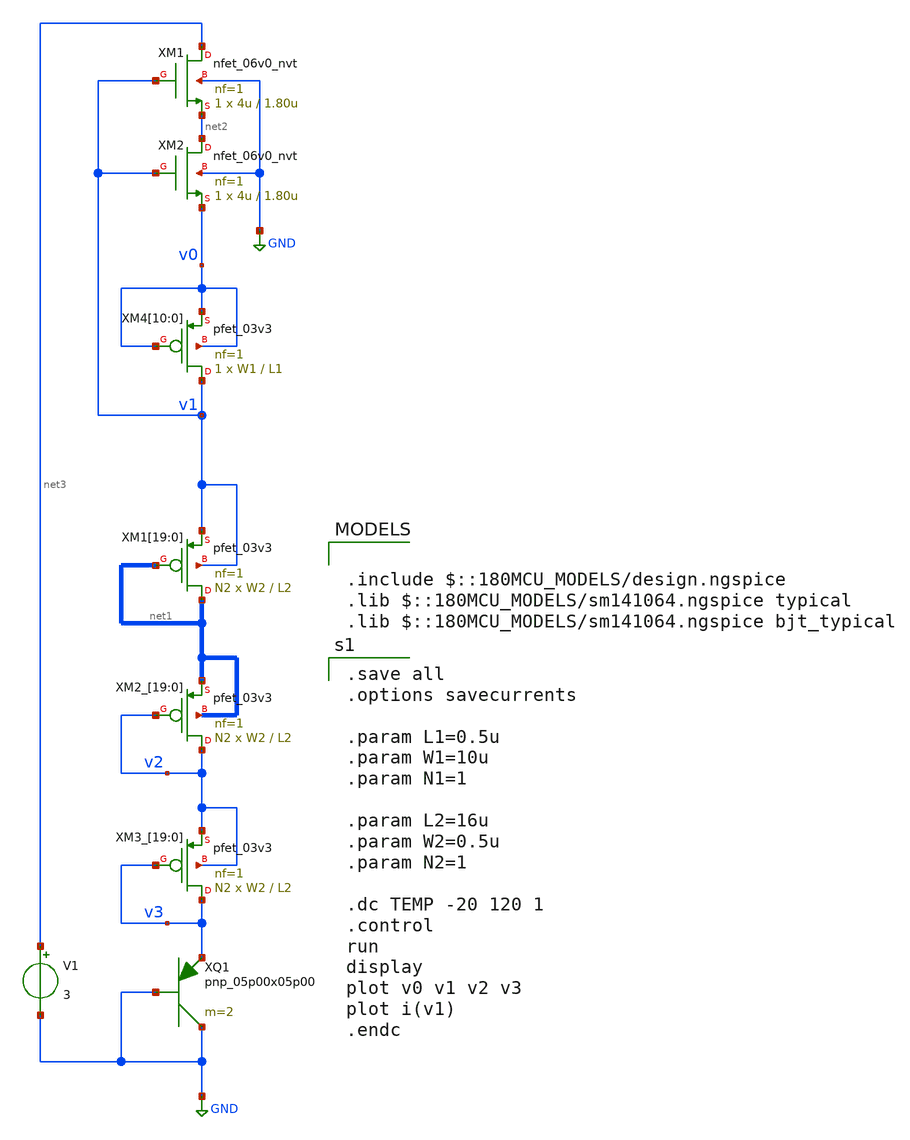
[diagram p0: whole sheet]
** sch_path: GF180/xschem/cmos_vref/Y.Ji_JSSC2019/s2_ztat1.sch
**.subckt s2_ztat1
XQ1 GND GND v3 pnp_05p00x05p00 m=2
V1 net3 GND 3
XM4[10] v1 v0 v0 v0 pfet_03v3 L=L1 W=W1 nf=1 ad='int((nf+1)/2) * W/nf * 0.18u' as='int((nf+2)/2) * W/nf * 0.18u'
+ pd='2*int((nf+1)/2) * (W/nf + 0.18u)' ps='2*int((nf+2)/2) * (W/nf + 0.18u)' nrd='0.18u / W' nrs='0.18u / W'
+ sa=0 sb=0 sd=0 m=1
XM4[9] v1 v0 v0 v0 pfet_03v3 L=L1 W=W1 nf=1 ad='int((nf+1)/2) * W/nf * 0.18u' as='int((nf+2)/2) * W/nf * 0.18u'
+ pd='2*int((nf+1)/2) * (W/nf + 0.18u)' ps='2*int((nf+2)/2) * (W/nf + 0.18u)' nrd='0.18u / W' nrs='0.18u / W'
+ sa=0 sb=0 sd=0 m=1
XM4[8] v1 v0 v0 v0 pfet_03v3 L=L1 W=W1 nf=1 ad='int((nf+1)/2) * W/nf * 0.18u' as='int((nf+2)/2) * W/nf * 0.18u'
+ pd='2*int((nf+1)/2) * (W/nf + 0.18u)' ps='2*int((nf+2)/2) * (W/nf + 0.18u)' nrd='0.18u / W' nrs='0.18u / W'
+ sa=0 sb=0 sd=0 m=1
XM4[7] v1 v0 v0 v0 pfet_03v3 L=L1 W=W1 nf=1 ad='int((nf+1)/2) * W/nf * 0.18u' as='int((nf+2)/2) * W/nf * 0.18u'
+ pd='2*int((nf+1)/2) * (W/nf + 0.18u)' ps='2*int((nf+2)/2) * (W/nf + 0.18u)' nrd='0.18u / W' nrs='0.18u / W'
+ sa=0 sb=0 sd=0 m=1
XM4[6] v1 v0 v0 v0 pfet_03v3 L=L1 W=W1 nf=1 ad='int((nf+1)/2) * W/nf * 0.18u' as='int((nf+2)/2) * W/nf * 0.18u'
+ pd='2*int((nf+1)/2) * (W/nf + 0.18u)' ps='2*int((nf+2)/2) * (W/nf + 0.18u)' nrd='0.18u / W' nrs='0.18u / W'
+ sa=0 sb=0 sd=0 m=1
XM4[5] v1 v0 v0 v0 pfet_03v3 L=L1 W=W1 nf=1 ad='int((nf+1)/2) * W/nf * 0.18u' as='int((nf+2)/2) * W/nf * 0.18u'
+ pd='2*int((nf+1)/2) * (W/nf + 0.18u)' ps='2*int((nf+2)/2) * (W/nf + 0.18u)' nrd='0.18u / W' nrs='0.18u / W'
+ sa=0 sb=0 sd=0 m=1
XM4[4] v1 v0 v0 v0 pfet_03v3 L=L1 W=W1 nf=1 ad='int((nf+1)/2) * W/nf * 0.18u' as='int((nf+2)/2) * W/nf * 0.18u'
+ pd='2*int((nf+1)/2) * (W/nf + 0.18u)' ps='2*int((nf+2)/2) * (W/nf + 0.18u)' nrd='0.18u / W' nrs='0.18u / W'
+ sa=0 sb=0 sd=0 m=1
XM4[3] v1 v0 v0 v0 pfet_03v3 L=L1 W=W1 nf=1 ad='int((nf+1)/2) * W/nf * 0.18u' as='int((nf+2)/2) * W/nf * 0.18u'
+ pd='2*int((nf+1)/2) * (W/nf + 0.18u)' ps='2*int((nf+2)/2) * (W/nf + 0.18u)' nrd='0.18u / W' nrs='0.18u / W'
+ sa=0 sb=0 sd=0 m=1
XM4[2] v1 v0 v0 v0 pfet_03v3 L=L1 W=W1 nf=1 ad='int((nf+1)/2) * W/nf * 0.18u' as='int((nf+2)/2) * W/nf * 0.18u'
+ pd='2*int((nf+1)/2) * (W/nf + 0.18u)' ps='2*int((nf+2)/2) * (W/nf + 0.18u)' nrd='0.18u / W' nrs='0.18u / W'
+ sa=0 sb=0 sd=0 m=1
XM4[1] v1 v0 v0 v0 pfet_03v3 L=L1 W=W1 nf=1 ad='int((nf+1)/2) * W/nf * 0.18u' as='int((nf+2)/2) * W/nf * 0.18u'
+ pd='2*int((nf+1)/2) * (W/nf + 0.18u)' ps='2*int((nf+2)/2) * (W/nf + 0.18u)' nrd='0.18u / W' nrs='0.18u / W'
+ sa=0 sb=0 sd=0 m=1
XM4[0] v1 v0 v0 v0 pfet_03v3 L=L1 W=W1 nf=1 ad='int((nf+1)/2) * W/nf * 0.18u' as='int((nf+2)/2) * W/nf * 0.18u'
+ pd='2*int((nf+1)/2) * (W/nf + 0.18u)' ps='2*int((nf+2)/2) * (W/nf + 0.18u)' nrd='0.18u / W' nrs='0.18u / W'
+ sa=0 sb=0 sd=0 m=1
XM2_[19] v2 v2 net1[19] net1[19] pfet_03v3 L=L2 W=W2 nf=1 ad='int((nf+1)/2) * W/nf * 0.18u' as='int((nf+2)/2) * W/nf * 0.18u'
+ pd='2*int((nf+1)/2) * (W/nf + 0.18u)' ps='2*int((nf+2)/2) * (W/nf + 0.18u)' nrd='0.18u / W' nrs='0.18u / W'
+ sa=0 sb=0 sd=0 m=N2
XM2_[18] v2 v2 net1[18] net1[18] pfet_03v3 L=L2 W=W2 nf=1 ad='int((nf+1)/2) * W/nf * 0.18u' as='int((nf+2)/2) * W/nf * 0.18u'
+ pd='2*int((nf+1)/2) * (W/nf + 0.18u)' ps='2*int((nf+2)/2) * (W/nf + 0.18u)' nrd='0.18u / W' nrs='0.18u / W'
+ sa=0 sb=0 sd=0 m=N2
XM2_[17] v2 v2 net1[17] net1[17] pfet_03v3 L=L2 W=W2 nf=1 ad='int((nf+1)/2) * W/nf * 0.18u' as='int((nf+2)/2) * W/nf * 0.18u'
+ pd='2*int((nf+1)/2) * (W/nf + 0.18u)' ps='2*int((nf+2)/2) * (W/nf + 0.18u)' nrd='0.18u / W' nrs='0.18u / W'
+ sa=0 sb=0 sd=0 m=N2
XM2_[16] v2 v2 net1[16] net1[16] pfet_03v3 L=L2 W=W2 nf=1 ad='int((nf+1)/2) * W/nf * 0.18u' as='int((nf+2)/2) * W/nf * 0.18u'
+ pd='2*int((nf+1)/2) * (W/nf + 0.18u)' ps='2*int((nf+2)/2) * (W/nf + 0.18u)' nrd='0.18u / W' nrs='0.18u / W'
+ sa=0 sb=0 sd=0 m=N2
XM2_[15] v2 v2 net1[15] net1[15] pfet_03v3 L=L2 W=W2 nf=1 ad='int((nf+1)/2) * W/nf * 0.18u' as='int((nf+2)/2) * W/nf * 0.18u'
+ pd='2*int((nf+1)/2) * (W/nf + 0.18u)' ps='2*int((nf+2)/2) * (W/nf + 0.18u)' nrd='0.18u / W' nrs='0.18u / W'
+ sa=0 sb=0 sd=0 m=N2
XM2_[14] v2 v2 net1[14] net1[14] pfet_03v3 L=L2 W=W2 nf=1 ad='int((nf+1)/2) * W/nf * 0.18u' as='int((nf+2)/2) * W/nf * 0.18u'
+ pd='2*int((nf+1)/2) * (W/nf + 0.18u)' ps='2*int((nf+2)/2) * (W/nf + 0.18u)' nrd='0.18u / W' nrs='0.18u / W'
+ sa=0 sb=0 sd=0 m=N2
XM2_[13] v2 v2 net1[13] net1[13] pfet_03v3 L=L2 W=W2 nf=1 ad='int((nf+1)/2) * W/nf * 0.18u' as='int((nf+2)/2) * W/nf * 0.18u'
+ pd='2*int((nf+1)/2) * (W/nf + 0.18u)' ps='2*int((nf+2)/2) * (W/nf + 0.18u)' nrd='0.18u / W' nrs='0.18u / W'
+ sa=0 sb=0 sd=0 m=N2
XM2_[12] v2 v2 net1[12] net1[12] pfet_03v3 L=L2 W=W2 nf=1 ad='int((nf+1)/2) * W/nf * 0.18u' as='int((nf+2)/2) * W/nf * 0.18u'
+ pd='2*int((nf+1)/2) * (W/nf + 0.18u)' ps='2*int((nf+2)/2) * (W/nf + 0.18u)' nrd='0.18u / W' nrs='0.18u / W'
+ sa=0 sb=0 sd=0 m=N2
XM2_[11] v2 v2 net1[11] net1[11] pfet_03v3 L=L2 W=W2 nf=1 ad='int((nf+1)/2) * W/nf * 0.18u' as='int((nf+2)/2) * W/nf * 0.18u'
+ pd='2*int((nf+1)/2) * (W/nf + 0.18u)' ps='2*int((nf+2)/2) * (W/nf + 0.18u)' nrd='0.18u / W' nrs='0.18u / W'
+ sa=0 sb=0 sd=0 m=N2
XM2_[10] v2 v2 net1[10] net1[10] pfet_03v3 L=L2 W=W2 nf=1 ad='int((nf+1)/2) * W/nf * 0.18u' as='int((nf+2)/2) * W/nf * 0.18u'
+ pd='2*int((nf+1)/2) * (W/nf + 0.18u)' ps='2*int((nf+2)/2) * (W/nf + 0.18u)' nrd='0.18u / W' nrs='0.18u / W'
+ sa=0 sb=0 sd=0 m=N2
XM2_[9] v2 v2 net1[9] net1[9] pfet_03v3 L=L2 W=W2 nf=1 ad='int((nf+1)/2) * W/nf * 0.18u' as='int((nf+2)/2) * W/nf * 0.18u'
+ pd='2*int((nf+1)/2) * (W/nf + 0.18u)' ps='2*int((nf+2)/2) * (W/nf + 0.18u)' nrd='0.18u / W' nrs='0.18u / W'
+ sa=0 sb=0 sd=0 m=N2
XM2_[8] v2 v2 net1[8] net1[8] pfet_03v3 L=L2 W=W2 nf=1 ad='int((nf+1)/2) * W/nf * 0.18u' as='int((nf+2)/2) * W/nf * 0.18u'
+ pd='2*int((nf+1)/2) * (W/nf + 0.18u)' ps='2*int((nf+2)/2) * (W/nf + 0.18u)' nrd='0.18u / W' nrs='0.18u / W'
+ sa=0 sb=0 sd=0 m=N2
XM2_[7] v2 v2 net1[7] net1[7] pfet_03v3 L=L2 W=W2 nf=1 ad='int((nf+1)/2) * W/nf * 0.18u' as='int((nf+2)/2) * W/nf * 0.18u'
+ pd='2*int((nf+1)/2) * (W/nf + 0.18u)' ps='2*int((nf+2)/2) * (W/nf + 0.18u)' nrd='0.18u / W' nrs='0.18u / W'
+ sa=0 sb=0 sd=0 m=N2
XM2_[6] v2 v2 net1[6] net1[6] pfet_03v3 L=L2 W=W2 nf=1 ad='int((nf+1)/2) * W/nf * 0.18u' as='int((nf+2)/2) * W/nf * 0.18u'
+ pd='2*int((nf+1)/2) * (W/nf + 0.18u)' ps='2*int((nf+2)/2) * (W/nf + 0.18u)' nrd='0.18u / W' nrs='0.18u / W'
+ sa=0 sb=0 sd=0 m=N2
XM2_[5] v2 v2 net1[5] net1[5] pfet_03v3 L=L2 W=W2 nf=1 ad='int((nf+1)/2) * W/nf * 0.18u' as='int((nf+2)/2) * W/nf * 0.18u'
+ pd='2*int((nf+1)/2) * (W/nf + 0.18u)' ps='2*int((nf+2)/2) * (W/nf + 0.18u)' nrd='0.18u / W' nrs='0.18u / W'
+ sa=0 sb=0 sd=0 m=N2
XM2_[4] v2 v2 net1[4] net1[4] pfet_03v3 L=L2 W=W2 nf=1 ad='int((nf+1)/2) * W/nf * 0.18u' as='int((nf+2)/2) * W/nf * 0.18u'
+ pd='2*int((nf+1)/2) * (W/nf + 0.18u)' ps='2*int((nf+2)/2) * (W/nf + 0.18u)' nrd='0.18u / W' nrs='0.18u / W'
+ sa=0 sb=0 sd=0 m=N2
XM2_[3] v2 v2 net1[3] net1[3] pfet_03v3 L=L2 W=W2 nf=1 ad='int((nf+1)/2) * W/nf * 0.18u' as='int((nf+2)/2) * W/nf * 0.18u'
+ pd='2*int((nf+1)/2) * (W/nf + 0.18u)' ps='2*int((nf+2)/2) * (W/nf + 0.18u)' nrd='0.18u / W' nrs='0.18u / W'
+ sa=0 sb=0 sd=0 m=N2
XM2_[2] v2 v2 net1[2] net1[2] pfet_03v3 L=L2 W=W2 nf=1 ad='int((nf+1)/2) * W/nf * 0.18u' as='int((nf+2)/2) * W/nf * 0.18u'
+ pd='2*int((nf+1)/2) * (W/nf + 0.18u)' ps='2*int((nf+2)/2) * (W/nf + 0.18u)' nrd='0.18u / W' nrs='0.18u / W'
+ sa=0 sb=0 sd=0 m=N2
XM2_[1] v2 v2 net1[1] net1[1] pfet_03v3 L=L2 W=W2 nf=1 ad='int((nf+1)/2) * W/nf * 0.18u' as='int((nf+2)/2) * W/nf * 0.18u'
+ pd='2*int((nf+1)/2) * (W/nf + 0.18u)' ps='2*int((nf+2)/2) * (W/nf + 0.18u)' nrd='0.18u / W' nrs='0.18u / W'
+ sa=0 sb=0 sd=0 m=N2
XM2_[0] v2 v2 net1[0] net1[0] pfet_03v3 L=L2 W=W2 nf=1 ad='int((nf+1)/2) * W/nf * 0.18u' as='int((nf+2)/2) * W/nf * 0.18u'
+ pd='2*int((nf+1)/2) * (W/nf + 0.18u)' ps='2*int((nf+2)/2) * (W/nf + 0.18u)' nrd='0.18u / W' nrs='0.18u / W'
+ sa=0 sb=0 sd=0 m=N2
XM3_[19] v3 v3 v2 v2 pfet_03v3 L=L2 W=W2 nf=1 ad='int((nf+1)/2) * W/nf * 0.18u' as='int((nf+2)/2) * W/nf * 0.18u'
+ pd='2*int((nf+1)/2) * (W/nf + 0.18u)' ps='2*int((nf+2)/2) * (W/nf + 0.18u)' nrd='0.18u / W' nrs='0.18u / W'
+ sa=0 sb=0 sd=0 m=N2
XM3_[18] v3 v3 v2 v2 pfet_03v3 L=L2 W=W2 nf=1 ad='int((nf+1)/2) * W/nf * 0.18u' as='int((nf+2)/2) * W/nf * 0.18u'
+ pd='2*int((nf+1)/2) * (W/nf + 0.18u)' ps='2*int((nf+2)/2) * (W/nf + 0.18u)' nrd='0.18u / W' nrs='0.18u / W'
+ sa=0 sb=0 sd=0 m=N2
XM3_[17] v3 v3 v2 v2 pfet_03v3 L=L2 W=W2 nf=1 ad='int((nf+1)/2) * W/nf * 0.18u' as='int((nf+2)/2) * W/nf * 0.18u'
+ pd='2*int((nf+1)/2) * (W/nf + 0.18u)' ps='2*int((nf+2)/2) * (W/nf + 0.18u)' nrd='0.18u / W' nrs='0.18u / W'
+ sa=0 sb=0 sd=0 m=N2
XM3_[16] v3 v3 v2 v2 pfet_03v3 L=L2 W=W2 nf=1 ad='int((nf+1)/2) * W/nf * 0.18u' as='int((nf+2)/2) * W/nf * 0.18u'
+ pd='2*int((nf+1)/2) * (W/nf + 0.18u)' ps='2*int((nf+2)/2) * (W/nf + 0.18u)' nrd='0.18u / W' nrs='0.18u / W'
+ sa=0 sb=0 sd=0 m=N2
XM3_[15] v3 v3 v2 v2 pfet_03v3 L=L2 W=W2 nf=1 ad='int((nf+1)/2) * W/nf * 0.18u' as='int((nf+2)/2) * W/nf * 0.18u'
+ pd='2*int((nf+1)/2) * (W/nf + 0.18u)' ps='2*int((nf+2)/2) * (W/nf + 0.18u)' nrd='0.18u / W' nrs='0.18u / W'
+ sa=0 sb=0 sd=0 m=N2
XM3_[14] v3 v3 v2 v2 pfet_03v3 L=L2 W=W2 nf=1 ad='int((nf+1)/2) * W/nf * 0.18u' as='int((nf+2)/2) * W/nf * 0.18u'
+ pd='2*int((nf+1)/2) * (W/nf + 0.18u)' ps='2*int((nf+2)/2) * (W/nf + 0.18u)' nrd='0.18u / W' nrs='0.18u / W'
+ sa=0 sb=0 sd=0 m=N2
XM3_[13] v3 v3 v2 v2 pfet_03v3 L=L2 W=W2 nf=1 ad='int((nf+1)/2) * W/nf * 0.18u' as='int((nf+2)/2) * W/nf * 0.18u'
+ pd='2*int((nf+1)/2) * (W/nf + 0.18u)' ps='2*int((nf+2)/2) * (W/nf + 0.18u)' nrd='0.18u / W' nrs='0.18u / W'
+ sa=0 sb=0 sd=0 m=N2
XM3_[12] v3 v3 v2 v2 pfet_03v3 L=L2 W=W2 nf=1 ad='int((nf+1)/2) * W/nf * 0.18u' as='int((nf+2)/2) * W/nf * 0.18u'
+ pd='2*int((nf+1)/2) * (W/nf + 0.18u)' ps='2*int((nf+2)/2) * (W/nf + 0.18u)' nrd='0.18u / W' nrs='0.18u / W'
+ sa=0 sb=0 sd=0 m=N2
XM3_[11] v3 v3 v2 v2 pfet_03v3 L=L2 W=W2 nf=1 ad='int((nf+1)/2) * W/nf * 0.18u' as='int((nf+2)/2) * W/nf * 0.18u'
+ pd='2*int((nf+1)/2) * (W/nf + 0.18u)' ps='2*int((nf+2)/2) * (W/nf + 0.18u)' nrd='0.18u / W' nrs='0.18u / W'
+ sa=0 sb=0 sd=0 m=N2
XM3_[10] v3 v3 v2 v2 pfet_03v3 L=L2 W=W2 nf=1 ad='int((nf+1)/2) * W/nf * 0.18u' as='int((nf+2)/2) * W/nf * 0.18u'
+ pd='2*int((nf+1)/2) * (W/nf + 0.18u)' ps='2*int((nf+2)/2) * (W/nf + 0.18u)' nrd='0.18u / W' nrs='0.18u / W'
+ sa=0 sb=0 sd=0 m=N2
XM3_[9] v3 v3 v2 v2 pfet_03v3 L=L2 W=W2 nf=1 ad='int((nf+1)/2) * W/nf * 0.18u' as='int((nf+2)/2) * W/nf * 0.18u'
+ pd='2*int((nf+1)/2) * (W/nf + 0.18u)' ps='2*int((nf+2)/2) * (W/nf + 0.18u)' nrd='0.18u / W' nrs='0.18u / W'
+ sa=0 sb=0 sd=0 m=N2
XM3_[8] v3 v3 v2 v2 pfet_03v3 L=L2 W=W2 nf=1 ad='int((nf+1)/2) * W/nf * 0.18u' as='int((nf+2)/2) * W/nf * 0.18u'
+ pd='2*int((nf+1)/2) * (W/nf + 0.18u)' ps='2*int((nf+2)/2) * (W/nf + 0.18u)' nrd='0.18u / W' nrs='0.18u / W'
+ sa=0 sb=0 sd=0 m=N2
XM3_[7] v3 v3 v2 v2 pfet_03v3 L=L2 W=W2 nf=1 ad='int((nf+1)/2) * W/nf * 0.18u' as='int((nf+2)/2) * W/nf * 0.18u'
+ pd='2*int((nf+1)/2) * (W/nf + 0.18u)' ps='2*int((nf+2)/2) * (W/nf + 0.18u)' nrd='0.18u / W' nrs='0.18u / W'
+ sa=0 sb=0 sd=0 m=N2
XM3_[6] v3 v3 v2 v2 pfet_03v3 L=L2 W=W2 nf=1 ad='int((nf+1)/2) * W/nf * 0.18u' as='int((nf+2)/2) * W/nf * 0.18u'
+ pd='2*int((nf+1)/2) * (W/nf + 0.18u)' ps='2*int((nf+2)/2) * (W/nf + 0.18u)' nrd='0.18u / W' nrs='0.18u / W'
+ sa=0 sb=0 sd=0 m=N2
XM3_[5] v3 v3 v2 v2 pfet_03v3 L=L2 W=W2 nf=1 ad='int((nf+1)/2) * W/nf * 0.18u' as='int((nf+2)/2) * W/nf * 0.18u'
+ pd='2*int((nf+1)/2) * (W/nf + 0.18u)' ps='2*int((nf+2)/2) * (W/nf + 0.18u)' nrd='0.18u / W' nrs='0.18u / W'
+ sa=0 sb=0 sd=0 m=N2
XM3_[4] v3 v3 v2 v2 pfet_03v3 L=L2 W=W2 nf=1 ad='int((nf+1)/2) * W/nf * 0.18u' as='int((nf+2)/2) * W/nf * 0.18u'
+ pd='2*int((nf+1)/2) * (W/nf + 0.18u)' ps='2*int((nf+2)/2) * (W/nf + 0.18u)' nrd='0.18u / W' nrs='0.18u / W'
+ sa=0 sb=0 sd=0 m=N2
XM3_[3] v3 v3 v2 v2 pfet_03v3 L=L2 W=W2 nf=1 ad='int((nf+1)/2) * W/nf * 0.18u' as='int((nf+2)/2) * W/nf * 0.18u'
+ pd='2*int((nf+1)/2) * (W/nf + 0.18u)' ps='2*int((nf+2)/2) * (W/nf + 0.18u)' nrd='0.18u / W' nrs='0.18u / W'
+ sa=0 sb=0 sd=0 m=N2
XM3_[2] v3 v3 v2 v2 pfet_03v3 L=L2 W=W2 nf=1 ad='int((nf+1)/2) * W/nf * 0.18u' as='int((nf+2)/2) * W/nf * 0.18u'
+ pd='2*int((nf+1)/2) * (W/nf + 0.18u)' ps='2*int((nf+2)/2) * (W/nf + 0.18u)' nrd='0.18u / W' nrs='0.18u / W'
+ sa=0 sb=0 sd=0 m=N2
XM3_[1] v3 v3 v2 v2 pfet_03v3 L=L2 W=W2 nf=1 ad='int((nf+1)/2) * W/nf * 0.18u' as='int((nf+2)/2) * W/nf * 0.18u'
+ pd='2*int((nf+1)/2) * (W/nf + 0.18u)' ps='2*int((nf+2)/2) * (W/nf + 0.18u)' nrd='0.18u / W' nrs='0.18u / W'
+ sa=0 sb=0 sd=0 m=N2
XM3_[0] v3 v3 v2 v2 pfet_03v3 L=L2 W=W2 nf=1 ad='int((nf+1)/2) * W/nf * 0.18u' as='int((nf+2)/2) * W/nf * 0.18u'
+ pd='2*int((nf+1)/2) * (W/nf + 0.18u)' ps='2*int((nf+2)/2) * (W/nf + 0.18u)' nrd='0.18u / W' nrs='0.18u / W'
+ sa=0 sb=0 sd=0 m=N2
XM1 net3 v1 net2 GND nfet_06v0_nvt L=1.80u W=4u nf=1 ad='int((nf+1)/2) * W/nf * 0.18u' as='int((nf+2)/2) * W/nf * 0.18u'
+ pd='2*int((nf+1)/2) * (W/nf + 0.18u)' ps='2*int((nf+2)/2) * (W/nf + 0.18u)' nrd='0.18u / W' nrs='0.18u / W'
+ sa=0 sb=0 sd=0 m=1
XM2 net2 v1 v0 GND nfet_06v0_nvt L=1.80u W=4u nf=1 ad='int((nf+1)/2) * W/nf * 0.18u' as='int((nf+2)/2) * W/nf * 0.18u'
+ pd='2*int((nf+1)/2) * (W/nf + 0.18u)' ps='2*int((nf+2)/2) * (W/nf + 0.18u)' nrd='0.18u / W' nrs='0.18u / W'
+ sa=0 sb=0 sd=0 m=1
XM1[19] net1[19] net1[19] v1 v1 pfet_03v3 L=L2 W=W2 nf=1 ad='int((nf+1)/2) * W/nf * 0.18u' as='int((nf+2)/2) * W/nf * 0.18u'
+ pd='2*int((nf+1)/2) * (W/nf + 0.18u)' ps='2*int((nf+2)/2) * (W/nf + 0.18u)' nrd='0.18u / W' nrs='0.18u / W'
+ sa=0 sb=0 sd=0 m=N2
XM1[18] net1[18] net1[18] v1 v1 pfet_03v3 L=L2 W=W2 nf=1 ad='int((nf+1)/2) * W/nf * 0.18u' as='int((nf+2)/2) * W/nf * 0.18u'
+ pd='2*int((nf+1)/2) * (W/nf + 0.18u)' ps='2*int((nf+2)/2) * (W/nf + 0.18u)' nrd='0.18u / W' nrs='0.18u / W'
+ sa=0 sb=0 sd=0 m=N2
XM1[17] net1[17] net1[17] v1 v1 pfet_03v3 L=L2 W=W2 nf=1 ad='int((nf+1)/2) * W/nf * 0.18u' as='int((nf+2)/2) * W/nf * 0.18u'
+ pd='2*int((nf+1)/2) * (W/nf + 0.18u)' ps='2*int((nf+2)/2) * (W/nf + 0.18u)' nrd='0.18u / W' nrs='0.18u / W'
+ sa=0 sb=0 sd=0 m=N2
XM1[16] net1[16] net1[16] v1 v1 pfet_03v3 L=L2 W=W2 nf=1 ad='int((nf+1)/2) * W/nf * 0.18u' as='int((nf+2)/2) * W/nf * 0.18u'
+ pd='2*int((nf+1)/2) * (W/nf + 0.18u)' ps='2*int((nf+2)/2) * (W/nf + 0.18u)' nrd='0.18u / W' nrs='0.18u / W'
+ sa=0 sb=0 sd=0 m=N2
XM1[15] net1[15] net1[15] v1 v1 pfet_03v3 L=L2 W=W2 nf=1 ad='int((nf+1)/2) * W/nf * 0.18u' as='int((nf+2)/2) * W/nf * 0.18u'
+ pd='2*int((nf+1)/2) * (W/nf + 0.18u)' ps='2*int((nf+2)/2) * (W/nf + 0.18u)' nrd='0.18u / W' nrs='0.18u / W'
+ sa=0 sb=0 sd=0 m=N2
XM1[14] net1[14] net1[14] v1 v1 pfet_03v3 L=L2 W=W2 nf=1 ad='int((nf+1)/2) * W/nf * 0.18u' as='int((nf+2)/2) * W/nf * 0.18u'
+ pd='2*int((nf+1)/2) * (W/nf + 0.18u)' ps='2*int((nf+2)/2) * (W/nf + 0.18u)' nrd='0.18u / W' nrs='0.18u / W'
+ sa=0 sb=0 sd=0 m=N2
XM1[13] net1[13] net1[13] v1 v1 pfet_03v3 L=L2 W=W2 nf=1 ad='int((nf+1)/2) * W/nf * 0.18u' as='int((nf+2)/2) * W/nf * 0.18u'
+ pd='2*int((nf+1)/2) * (W/nf + 0.18u)' ps='2*int((nf+2)/2) * (W/nf + 0.18u)' nrd='0.18u / W' nrs='0.18u / W'
+ sa=0 sb=0 sd=0 m=N2
XM1[12] net1[12] net1[12] v1 v1 pfet_03v3 L=L2 W=W2 nf=1 ad='int((nf+1)/2) * W/nf * 0.18u' as='int((nf+2)/2) * W/nf * 0.18u'
+ pd='2*int((nf+1)/2) * (W/nf + 0.18u)' ps='2*int((nf+2)/2) * (W/nf + 0.18u)' nrd='0.18u / W' nrs='0.18u / W'
+ sa=0 sb=0 sd=0 m=N2
XM1[11] net1[11] net1[11] v1 v1 pfet_03v3 L=L2 W=W2 nf=1 ad='int((nf+1)/2) * W/nf * 0.18u' as='int((nf+2)/2) * W/nf * 0.18u'
+ pd='2*int((nf+1)/2) * (W/nf + 0.18u)' ps='2*int((nf+2)/2) * (W/nf + 0.18u)' nrd='0.18u / W' nrs='0.18u / W'
+ sa=0 sb=0 sd=0 m=N2
XM1[10] net1[10] net1[10] v1 v1 pfet_03v3 L=L2 W=W2 nf=1 ad='int((nf+1)/2) * W/nf * 0.18u' as='int((nf+2)/2) * W/nf * 0.18u'
+ pd='2*int((nf+1)/2) * (W/nf + 0.18u)' ps='2*int((nf+2)/2) * (W/nf + 0.18u)' nrd='0.18u / W' nrs='0.18u / W'
+ sa=0 sb=0 sd=0 m=N2
XM1[9] net1[9] net1[9] v1 v1 pfet_03v3 L=L2 W=W2 nf=1 ad='int((nf+1)/2) * W/nf * 0.18u' as='int((nf+2)/2) * W/nf * 0.18u'
+ pd='2*int((nf+1)/2) * (W/nf + 0.18u)' ps='2*int((nf+2)/2) * (W/nf + 0.18u)' nrd='0.18u / W' nrs='0.18u / W'
+ sa=0 sb=0 sd=0 m=N2
XM1[8] net1[8] net1[8] v1 v1 pfet_03v3 L=L2 W=W2 nf=1 ad='int((nf+1)/2) * W/nf * 0.18u' as='int((nf+2)/2) * W/nf * 0.18u'
+ pd='2*int((nf+1)/2) * (W/nf + 0.18u)' ps='2*int((nf+2)/2) * (W/nf + 0.18u)' nrd='0.18u / W' nrs='0.18u / W'
+ sa=0 sb=0 sd=0 m=N2
XM1[7] net1[7] net1[7] v1 v1 pfet_03v3 L=L2 W=W2 nf=1 ad='int((nf+1)/2) * W/nf * 0.18u' as='int((nf+2)/2) * W/nf * 0.18u'
+ pd='2*int((nf+1)/2) * (W/nf + 0.18u)' ps='2*int((nf+2)/2) * (W/nf + 0.18u)' nrd='0.18u / W' nrs='0.18u / W'
+ sa=0 sb=0 sd=0 m=N2
XM1[6] net1[6] net1[6] v1 v1 pfet_03v3 L=L2 W=W2 nf=1 ad='int((nf+1)/2) * W/nf * 0.18u' as='int((nf+2)/2) * W/nf * 0.18u'
+ pd='2*int((nf+1)/2) * (W/nf + 0.18u)' ps='2*int((nf+2)/2) * (W/nf + 0.18u)' nrd='0.18u / W' nrs='0.18u / W'
+ sa=0 sb=0 sd=0 m=N2
XM1[5] net1[5] net1[5] v1 v1 pfet_03v3 L=L2 W=W2 nf=1 ad='int((nf+1)/2) * W/nf * 0.18u' as='int((nf+2)/2) * W/nf * 0.18u'
+ pd='2*int((nf+1)/2) * (W/nf + 0.18u)' ps='2*int((nf+2)/2) * (W/nf + 0.18u)' nrd='0.18u / W' nrs='0.18u / W'
+ sa=0 sb=0 sd=0 m=N2
XM1[4] net1[4] net1[4] v1 v1 pfet_03v3 L=L2 W=W2 nf=1 ad='int((nf+1)/2) * W/nf * 0.18u' as='int((nf+2)/2) * W/nf * 0.18u'
+ pd='2*int((nf+1)/2) * (W/nf + 0.18u)' ps='2*int((nf+2)/2) * (W/nf + 0.18u)' nrd='0.18u / W' nrs='0.18u / W'
+ sa=0 sb=0 sd=0 m=N2
XM1[3] net1[3] net1[3] v1 v1 pfet_03v3 L=L2 W=W2 nf=1 ad='int((nf+1)/2) * W/nf * 0.18u' as='int((nf+2)/2) * W/nf * 0.18u'
+ pd='2*int((nf+1)/2) * (W/nf + 0.18u)' ps='2*int((nf+2)/2) * (W/nf + 0.18u)' nrd='0.18u / W' nrs='0.18u / W'
+ sa=0 sb=0 sd=0 m=N2
XM1[2] net1[2] net1[2] v1 v1 pfet_03v3 L=L2 W=W2 nf=1 ad='int((nf+1)/2) * W/nf * 0.18u' as='int((nf+2)/2) * W/nf * 0.18u'
+ pd='2*int((nf+1)/2) * (W/nf + 0.18u)' ps='2*int((nf+2)/2) * (W/nf + 0.18u)' nrd='0.18u / W' nrs='0.18u / W'
+ sa=0 sb=0 sd=0 m=N2
XM1[1] net1[1] net1[1] v1 v1 pfet_03v3 L=L2 W=W2 nf=1 ad='int((nf+1)/2) * W/nf * 0.18u' as='int((nf+2)/2) * W/nf * 0.18u'
+ pd='2*int((nf+1)/2) * (W/nf + 0.18u)' ps='2*int((nf+2)/2) * (W/nf + 0.18u)' nrd='0.18u / W' nrs='0.18u / W'
+ sa=0 sb=0 sd=0 m=N2
XM1[0] net1[0] net1[0] v1 v1 pfet_03v3 L=L2 W=W2 nf=1 ad='int((nf+1)/2) * W/nf * 0.18u' as='int((nf+2)/2) * W/nf * 0.18u'
+ pd='2*int((nf+1)/2) * (W/nf + 0.18u)' ps='2*int((nf+2)/2) * (W/nf + 0.18u)' nrd='0.18u / W' nrs='0.18u / W'
+ sa=0 sb=0 sd=0 m=N2
**** begin user architecture code

.include $::180MCU_MODELS/design.ngspice
.lib $::180MCU_MODELS/sm141064.ngspice typical
.lib $::180MCU_MODELS/sm141064.ngspice bjt_typical


.save all
.options savecurrents

.param L1=0.5u
.param W1=10u
.param N1=1

.param L2=16u
.param W2=0.5u
.param N2=1

.dc TEMP -20 120 1
.control
run
display
plot v0 v1 v2 v3
plot i(v1)
.endc


**** end user architecture code
**.ends
.GLOBAL GND
.end
